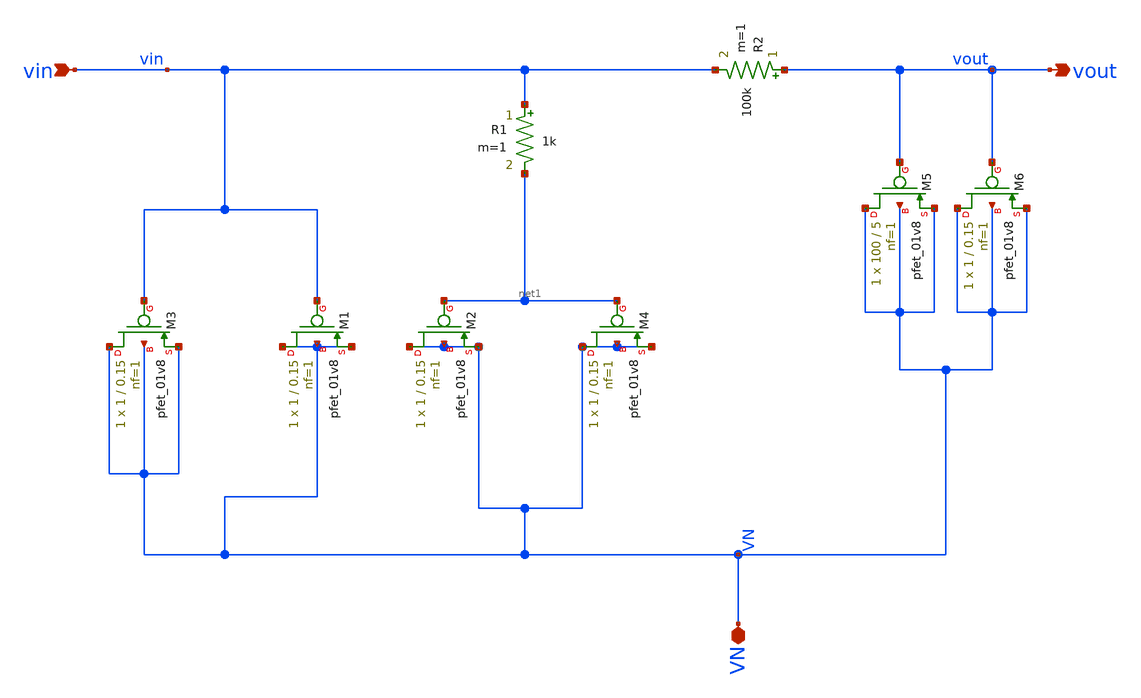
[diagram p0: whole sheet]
** sch_path: git_11/LOOP_FILTER.sch
**.subckt LOOP_FILTER VN vin vout
*.iopin VN
*.ipin vin
*.opin vout
R1 vin net1 1k m=1
R2 vout vin 100k m=1
XM3 VN vin VN VN sky130_fd_pr__pfet_01v8 L=0.15 W=1 nf=1 ad='int((nf+1)/2) * W/nf * 0.29' as='int((nf+2)/2) * W/nf * 0.29'
+ pd='2*int((nf+1)/2) * (W/nf + 0.29)' ps='2*int((nf+2)/2) * (W/nf + 0.29)' nrd='0.29 / W' nrs='0.29 / W'
+ sa=0 sb=0 sd=0 mult=1 m=1
XM1 VN vin VN VN sky130_fd_pr__pfet_01v8 L=0.15 W=1 nf=1 ad='int((nf+1)/2) * W/nf * 0.29' as='int((nf+2)/2) * W/nf * 0.29'
+ pd='2*int((nf+1)/2) * (W/nf + 0.29)' ps='2*int((nf+2)/2) * (W/nf + 0.29)' nrd='0.29 / W' nrs='0.29 / W'
+ sa=0 sb=0 sd=0 mult=1 m=1
XM2 VN net1 VN VN sky130_fd_pr__pfet_01v8 L=0.15 W=1 nf=1 ad='int((nf+1)/2) * W/nf * 0.29' as='int((nf+2)/2) * W/nf * 0.29'
+ pd='2*int((nf+1)/2) * (W/nf + 0.29)' ps='2*int((nf+2)/2) * (W/nf + 0.29)' nrd='0.29 / W' nrs='0.29 / W'
+ sa=0 sb=0 sd=0 mult=1 m=1
XM4 VN net1 VN VN sky130_fd_pr__pfet_01v8 L=0.15 W=1 nf=1 ad='int((nf+1)/2) * W/nf * 0.29' as='int((nf+2)/2) * W/nf * 0.29'
+ pd='2*int((nf+1)/2) * (W/nf + 0.29)' ps='2*int((nf+2)/2) * (W/nf + 0.29)' nrd='0.29 / W' nrs='0.29 / W'
+ sa=0 sb=0 sd=0 mult=1 m=1
XM5 VN vout VN VN sky130_fd_pr__pfet_01v8 L=5 W=100 nf=1 ad='int((nf+1)/2) * W/nf * 0.29' as='int((nf+2)/2) * W/nf * 0.29'
+ pd='2*int((nf+1)/2) * (W/nf + 0.29)' ps='2*int((nf+2)/2) * (W/nf + 0.29)' nrd='0.29 / W' nrs='0.29 / W'
+ sa=0 sb=0 sd=0 mult=1 m=1
XM6 VN vout VN VN sky130_fd_pr__pfet_01v8 L=0.15 W=1 nf=1 ad='int((nf+1)/2) * W/nf * 0.29' as='int((nf+2)/2) * W/nf * 0.29'
+ pd='2*int((nf+1)/2) * (W/nf + 0.29)' ps='2*int((nf+2)/2) * (W/nf + 0.29)' nrd='0.29 / W' nrs='0.29 / W'
+ sa=0 sb=0 sd=0 mult=1 m=1
**.ends
.end
